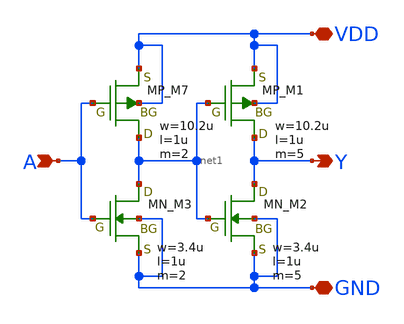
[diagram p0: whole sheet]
** sch_path: libs.tech/xschem/TR-1um_stdcell/CLKBUF_X1.sch
**.subckt CLKBUF_X1 A Y VDD GND
*.ipin A
*.opin Y
*.iopin VDD
*.iopin GND
XM7 net1 A VDD VDD PMOS w=10.2u l=1u nrd=0 nrs=0 m=2
XM1 Y net1 VDD VDD PMOS w=10.2u l=1u nrd=0 nrs=0 m=5
XM3 net1 A GND GND NMOS w=3.4u l=1u nrd=0 nrs=0 m=2
XM2 Y net1 GND GND NMOS w=3.4u l=1u nrd=0 nrs=0 m=5
**.ends
.end
